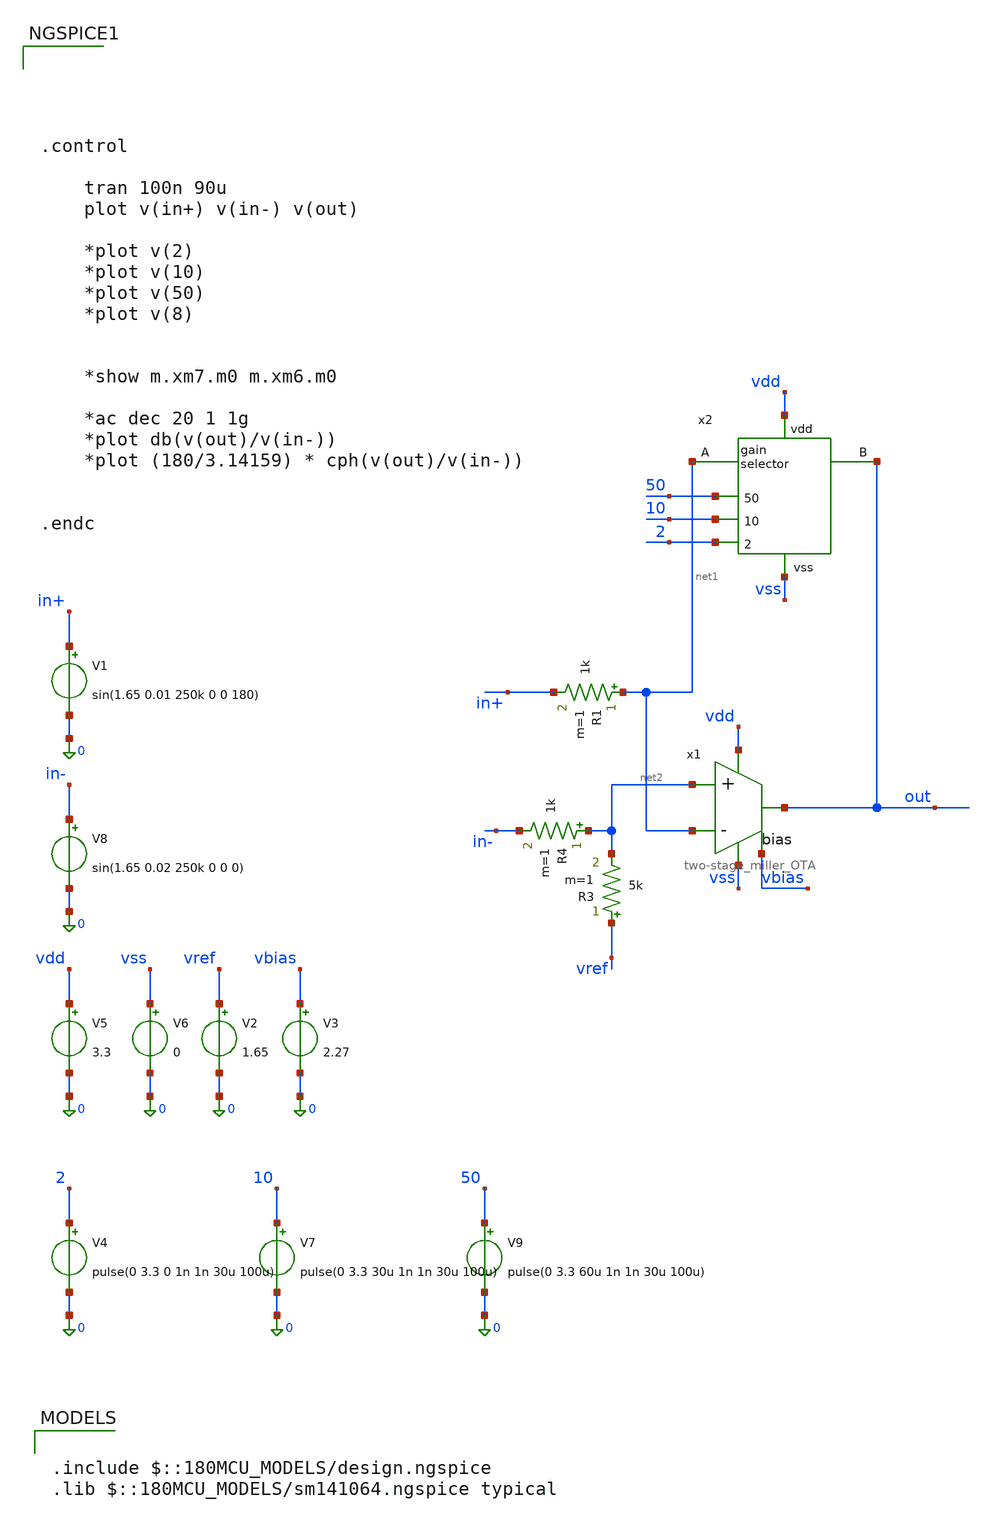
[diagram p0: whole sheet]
** sch_path: simulation/testbench_analog/PGA/PGA_transient.sch
**.subckt PGA_transient
V5 vdd 0 3.3
V6 vss 0 0
V8 in- 0 sin(1.65 0.02 250k 0 0 0)
V1 in+ 0 sin(1.65 0.01 250k 0 0 180)
R1 net1 in+ 1k m=1
V2 vref 0 1.65
R3 vref net2 5k m=1
R4 net2 in- 1k m=1
V3 vbias 0 2.27
x1 vdd out net2 net1 vbias vss two-stage_miller_OTA
V4 2 0 pulse(0 3.3 0 1n 1n 30u 100u)
V7 10 0 pulse(0 3.3 30u 1n 1n 30u 100u)
V9 50 0 pulse(0 3.3 60u 1n 1n 30u 100u)
x2 vdd vss 50 net1 10 out 2 gain_selector
**** begin user architecture code





.control

	tran 100n 90u
	plot v(in+) v(in-) v(out)

	*plot v(2)
	*plot v(10)
	*plot v(50)
	*plot v(8)


	*show m.xm7.m0 m.xm6.m0

	*ac dec 20 1 1g
	*plot db(v(out)/v(in-))
	*plot (180/3.14159) * cph(v(out)/v(in-))


.endc



.include $::180MCU_MODELS/design.ngspice
.lib $::180MCU_MODELS/sm141064.ngspice typical

**** end user architecture code
**.ends

* expanding   symbol:  acoustic_ranger_2026/two-stage_miller_OTA.sym # of pins=6
** sym_path: design/analog/OTA/two-stage_miller_OTA.sym
** sch_path: design/analog/OTA/two-stage_miller_OTA.sch
.subckt two-stage_miller_OTA vdd out in+ in- bias vss
*.ipin in+
*.ipin in-
*.opin out
*.iopin vdd
*.iopin vss
*.ipin bias
XM1 net2 in- net1 vdd pfet_03v3 L=1u W=6.2u nf=1 ad='int((nf+1)/2) * W/nf * 0.18u' as='int((nf+2)/2) * W/nf * 0.18u'
+ pd='2*int((nf+1)/2) * (W/nf + 0.18u)' ps='2*int((nf+2)/2) * (W/nf + 0.18u)' nrd='0.18u / W' nrs='0.18u / W'
+ sa=0 sb=0 sd=0 m=8
XM2 net3 in+ net1 vdd pfet_03v3 L=1u W=6.2u nf=1 ad='int((nf+1)/2) * W/nf * 0.18u' as='int((nf+2)/2) * W/nf * 0.18u'
+ pd='2*int((nf+1)/2) * (W/nf + 0.18u)' ps='2*int((nf+2)/2) * (W/nf + 0.18u)' nrd='0.18u / W' nrs='0.18u / W'
+ sa=0 sb=0 sd=0 m=8
XM14 net3 net2 vss vss nfet_03v3 L=3u W=7.7u nf=4 ad='int((nf+1)/2) * W/nf * 0.18u' as='int((nf+2)/2) * W/nf * 0.18u'
+ pd='2*int((nf+1)/2) * (W/nf + 0.18u)' ps='2*int((nf+2)/2) * (W/nf + 0.18u)' nrd='0.18u / W' nrs='0.18u / W'
+ sa=0 sb=0 sd=0 m=2
XM15 net2 net2 vss vss nfet_03v3 L=3u W=7.7u nf=4 ad='int((nf+1)/2) * W/nf * 0.18u' as='int((nf+2)/2) * W/nf * 0.18u'
+ pd='2*int((nf+1)/2) * (W/nf + 0.18u)' ps='2*int((nf+2)/2) * (W/nf + 0.18u)' nrd='0.18u / W' nrs='0.18u / W'
+ sa=0 sb=0 sd=0 m=2
XM3 out net3 vss vss nfet_03v3 L=3u W=7.7u nf=4 ad='int((nf+1)/2) * W/nf * 0.18u' as='int((nf+2)/2) * W/nf * 0.18u'
+ pd='2*int((nf+1)/2) * (W/nf + 0.18u)' ps='2*int((nf+2)/2) * (W/nf + 0.18u)' nrd='0.18u / W' nrs='0.18u / W'
+ sa=0 sb=0 sd=0 m=12
C1 out net3 5p m=1
XM4 net1 bias vdd vdd pfet_03v3 L=20u W=25.3u nf=2 ad='int((nf+1)/2) * W/nf * 0.18u' as='int((nf+2)/2) * W/nf * 0.18u'
+ pd='2*int((nf+1)/2) * (W/nf + 0.18u)' ps='2*int((nf+2)/2) * (W/nf + 0.18u)' nrd='0.18u / W' nrs='0.18u / W'
+ sa=0 sb=0 sd=0 m=2
XM5 out bias vdd vdd pfet_03v3 L=20u W=25.3u nf=2 ad='int((nf+1)/2) * W/nf * 0.18u' as='int((nf+2)/2) * W/nf * 0.18u'
+ pd='2*int((nf+1)/2) * (W/nf + 0.18u)' ps='2*int((nf+2)/2) * (W/nf + 0.18u)' nrd='0.18u / W' nrs='0.18u / W'
+ sa=0 sb=0 sd=0 m=6
.ends


* expanding   symbol:  acoustic-ranger-dvl-processor/design/analog/PGA/gain_selector.sym # of pins=7
** sym_path: design/analog/PGA/gain_selector.sym
** sch_path: design/analog/PGA/gain_selector.sch
.subckt gain_selector vdd vss 50 A 10 B 2
*.iopin A
*.iopin B
*.ipin 2
*.ipin 10
*.ipin 50
*.iopin vdd
*.iopin vss
x9 A 2b 2 vdd vss net1 Transmission_Gate
R5 net1 B 2k m=1
x10 A 10b 10 vdd vss net2 Transmission_Gate
R6 net2 B 10k m=1
x11 A 50b 50 vdd vss net3 Transmission_Gate
R7 net3 B 50k m=1
XM9 50b 50 vdd vdd pfet_03v3 L=0.28u W=2u nf=1 ad='int((nf+1)/2) * W/nf * 0.18u' as='int((nf+2)/2) * W/nf * 0.18u'
+ pd='2*int((nf+1)/2) * (W/nf + 0.18u)' ps='2*int((nf+2)/2) * (W/nf + 0.18u)' nrd='0.18u / W' nrs='0.18u / W'
+ sa=0 sb=0 sd=0 m=1
XM10 50b 50 vss vss nfet_03v3 L=0.28u W=1u nf=1 ad='int((nf+1)/2) * W/nf * 0.18u' as='int((nf+2)/2) * W/nf * 0.18u'
+ pd='2*int((nf+1)/2) * (W/nf + 0.18u)' ps='2*int((nf+2)/2) * (W/nf + 0.18u)' nrd='0.18u / W' nrs='0.18u / W'
+ sa=0 sb=0 sd=0 m=1
XM11 10b 10 vdd vdd pfet_03v3 L=0.28u W=2u nf=1 ad='int((nf+1)/2) * W/nf * 0.18u' as='int((nf+2)/2) * W/nf * 0.18u'
+ pd='2*int((nf+1)/2) * (W/nf + 0.18u)' ps='2*int((nf+2)/2) * (W/nf + 0.18u)' nrd='0.18u / W' nrs='0.18u / W'
+ sa=0 sb=0 sd=0 m=1
XM12 10b 10 vss vss nfet_03v3 L=0.28u W=1u nf=1 ad='int((nf+1)/2) * W/nf * 0.18u' as='int((nf+2)/2) * W/nf * 0.18u'
+ pd='2*int((nf+1)/2) * (W/nf + 0.18u)' ps='2*int((nf+2)/2) * (W/nf + 0.18u)' nrd='0.18u / W' nrs='0.18u / W'
+ sa=0 sb=0 sd=0 m=1
XM13 2b 2 vdd vdd pfet_03v3 L=0.28u W=2u nf=1 ad='int((nf+1)/2) * W/nf * 0.18u' as='int((nf+2)/2) * W/nf * 0.18u'
+ pd='2*int((nf+1)/2) * (W/nf + 0.18u)' ps='2*int((nf+2)/2) * (W/nf + 0.18u)' nrd='0.18u / W' nrs='0.18u / W'
+ sa=0 sb=0 sd=0 m=1
XM14 2b 2 vss vss nfet_03v3 L=0.28u W=1u nf=1 ad='int((nf+1)/2) * W/nf * 0.18u' as='int((nf+2)/2) * W/nf * 0.18u'
+ pd='2*int((nf+1)/2) * (W/nf + 0.18u)' ps='2*int((nf+2)/2) * (W/nf + 0.18u)' nrd='0.18u / W' nrs='0.18u / W'
+ sa=0 sb=0 sd=0 m=1
.ends


* expanding   symbol:  Transmission_Gate.sym # of pins=6
** sym_path: design/analog/transmission_gate/Transmission_Gate.sym
** sch_path: design/analog/transmission_gate/Transmission_Gate.sch
.subckt Transmission_Gate A en_b en vdd vss B
*.ipin en_b
*.iopin A
*.iopin B
*.ipin en
*.iopin vdd
*.iopin vss
XM1 B en_b A vdd pfet_03v3 L=0.28u W=20u nf=10 ad='int((nf+1)/2) * W/nf * 0.18u' as='int((nf+2)/2) * W/nf * 0.18u'
+ pd='2*int((nf+1)/2) * (W/nf + 0.18u)' ps='2*int((nf+2)/2) * (W/nf + 0.18u)' nrd='0.18u / W' nrs='0.18u / W'
+ sa=0 sb=0 sd=0 m=8
XM2 A en B vss nfet_03v3 L=0.28u W=10u nf=5 ad='int((nf+1)/2) * W/nf * 0.18u' as='int((nf+2)/2) * W/nf * 0.18u'
+ pd='2*int((nf+1)/2) * (W/nf + 0.18u)' ps='2*int((nf+2)/2) * (W/nf + 0.18u)' nrd='0.18u / W' nrs='0.18u / W'
+ sa=0 sb=0 sd=0 m=8
.ends

.end
